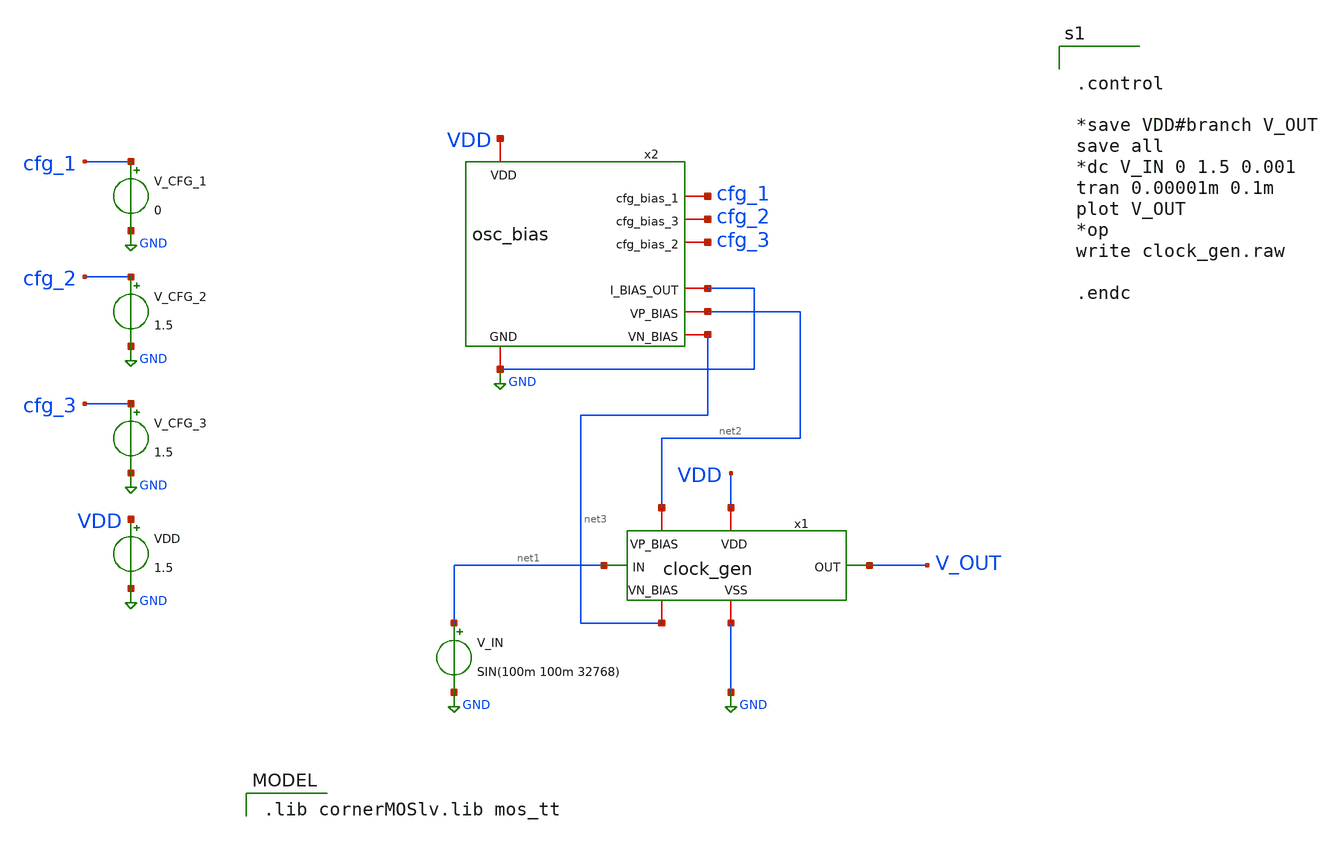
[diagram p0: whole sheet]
** sch_path: clock_gen_tb.sch
**.subckt clock_gen_tb
VDD VDD GND 1.5
V_IN net1 GND SIN(100m 100m 32768)
x1 VDD net1 V_OUT GND net2 net3 clock_gen
x2 VDD cfg_1 cfg_2 cfg_3 GND GND net2 net3 osc_bias
V_CFG_1 cfg_1 GND 0
V_CFG_2 cfg_2 GND 1.5
V_CFG_3 cfg_3 GND 1.5
**** begin user architecture code
 .lib cornerMOSlv.lib mos_tt



.control

*save VDD#branch V_OUT
save all
*dc V_IN 0 1.5 0.001
tran 0.00001m 0.1m
plot V_OUT
*op
write clock_gen.raw

.endc


**** end user architecture code
**.ends

* expanding   symbol:  clock_gen.sym # of pins=6
** sym_path: clock_gen.sym
** sch_path: clock_gen.sch
.subckt clock_gen VDD IN OUT VSS VP_BIAS VN_BIAS
*.iopin VSS
*.iopin VDD
*.ipin IN
*.opin OUT
*.ipin VP_BIAS
*.ipin VN_BIAS
XM1 stage_1 net1 net3 VSS sg13_lv_nmos w=1u l=2u ng=1 m=1 mm_ok=1
XM2 stage_1 net1 net2 VDD sg13_lv_pmos w=2u l=2u ng=1 m=1 mm_ok=1
R1 stage_1 net1 1G m=1
C1 IN net1 100p m=1
XM3 stage_2 stage_1 net5 VSS sg13_lv_nmos w=1u l=2u ng=1 m=1 mm_ok=1
XM4 stage_2 stage_1 net4 VDD sg13_lv_pmos w=2u l=2u ng=1 m=1 mm_ok=1
XM5 OUT stage_2 net7 VSS sg13_lv_nmos w=0.36u l=0.5u ng=1 m=1 mm_ok=1
XM6 OUT stage_2 net6 VDD sg13_lv_pmos w=0.72u l=0.5u ng=1 m=1 mm_ok=1
XM7 net2 VP_BIAS VDD VDD sg13_lv_pmos w=2u l=2u ng=1 m=1 mm_ok=1
XM8 net3 VN_BIAS VSS VSS sg13_lv_nmos w=1u l=2u ng=1 m=1 mm_ok=1
XM9 net4 VP_BIAS VDD VDD sg13_lv_pmos w=2u l=2u ng=1 m=1 mm_ok=1
XM10 net5 VN_BIAS VSS VSS sg13_lv_nmos w=1u l=2u ng=1 m=1 mm_ok=1
XM11 net6 VP_BIAS VDD VDD sg13_lv_pmos w=2u l=2u ng=1 m=1 mm_ok=1
XM12 net7 VN_BIAS VSS VSS sg13_lv_nmos w=1u l=2u ng=1 m=1 mm_ok=1
.ends


* expanding   symbol:  osc_bias.sym # of pins=8
** sym_path: osc_bias.sym
** sch_path: osc_bias.sch
.subckt osc_bias VDD cfg_bias_1 cfg_bias_3 cfg_bias_2 GND I_BIAS_OUT VP_BIAS VN_BIAS
*.iopin VDD
*.iopin GND
*.iopin I_BIAS_OUT
*.iopin cfg_bias_1
*.iopin cfg_bias_2
*.iopin cfg_bias_3
*.opin VN_BIAS
*.opin VP_BIAS
XM1 VP_BIAS VP_BIAS VDD VDD sg13_lv_pmos w=1u l=10u ng=1 m=1 mm_ok=1
XM3 VP_BIAS VP_BIAS net1 VN_BIAS sg13_lv_nmos w=0.25u l=10u ng=1 m=1 mm_ok=1
XM4 net1 net1 net2 VN_BIAS sg13_lv_nmos w=0.25u l=10u ng=1 m=1 mm_ok=1
XM5 net2 net2 VN_BIAS VN_BIAS sg13_lv_nmos w=0.25u l=10u ng=1 m=1 mm_ok=1
XM2 net6 VP_BIAS VDD VDD sg13_lv_pmos w=0.5u l=10u ng=1 m=1 mm_ok=1
XM6 I_BIAS_OUT cfg_bias_1 net6 VDD sg13_lv_pmos w=0.5u l=5u ng=1 m=1 mm_ok=1
XM7 net3 VP_BIAS VDD VDD sg13_lv_pmos w=0.5u l=10u ng=1 m=1 mm_ok=1
XM8 net4 VP_BIAS VDD VDD sg13_lv_pmos w=0.5u l=10u ng=1 m=1 mm_ok=1
XM9 I_BIAS_OUT cfg_bias_2 net3 VDD sg13_lv_pmos w=0.5u l=10u ng=1 m=1 mm_ok=1
XM10 I_BIAS_OUT cfg_bias_3 net4 VDD sg13_lv_pmos w=0.5u l=10u ng=1 m=1 mm_ok=1
XM11 VN_BIAS VN_BIAS net5 VN_BIAS sg13_lv_nmos w=0.25u l=10u ng=1 m=1 mm_ok=1
Vmeas net5 GND 0
.save i(vmeas)
.ends

.GLOBAL GND
.end
